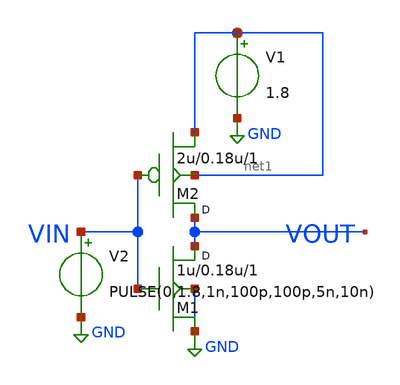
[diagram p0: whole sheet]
** sch_path: My_Inverter/inverter_test.sch
**.subckt inverter_test
M1 VOUT VIN GND GND nmos w=1u l=0.18u m=1
M2 VOUT VIN net1 net1 pmos w=2u l=0.18u m=1
V1 net1 GND 1.8
V2 VIN GND PULSE(0,1.8,1n,100p,100p,5n,10n)
**.ends
.GLOBAL GND
.end
